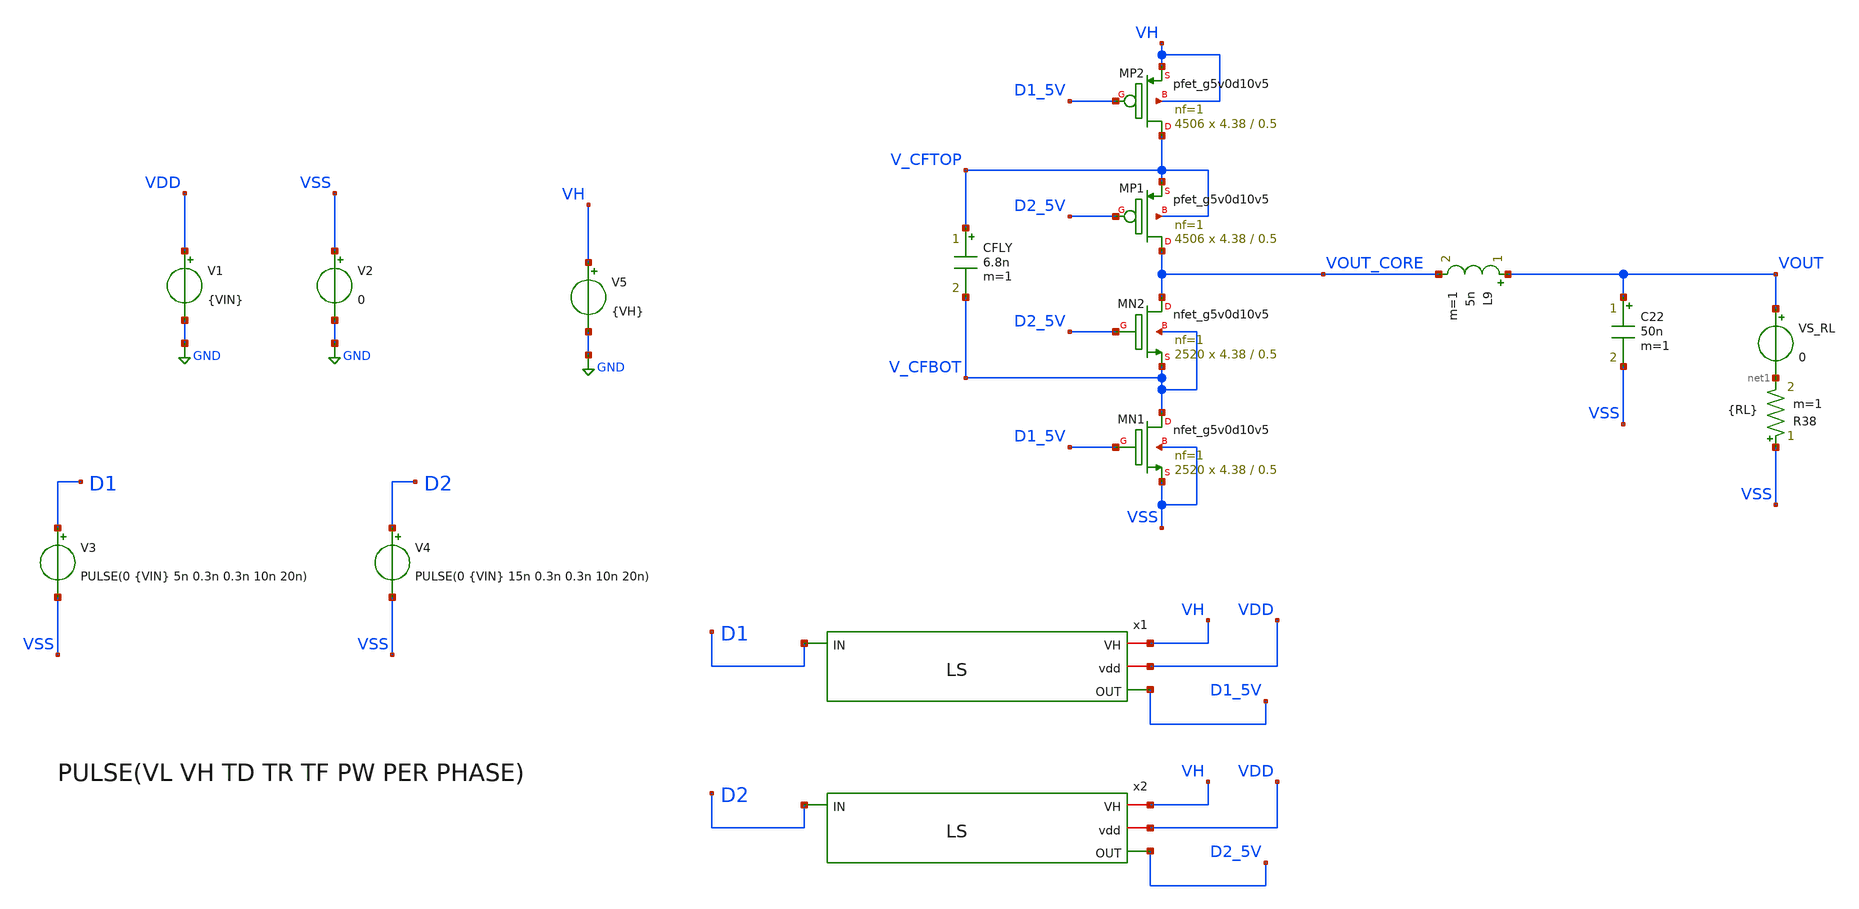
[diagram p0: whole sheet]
** sch_path: xschem/dev_switches/DCDC_v1p3_100MHz_NMOS_PMOS_jm.sch
**.subckt DCDC_v1p3_100MHz_NMOS_PMOS_jm
XMN2 VOUT_CORE D2_5V V_CFBOT V_CFBOT sky130_fd_pr__nfet_g5v0d10v5 L=0.5 W=4.38 nf=1 ad='int((nf+1)/2) * W/nf * 0.29'
+ as='int((nf+2)/2) * W/nf * 0.29' pd='2*int((nf+1)/2) * (W/nf + 0.29)' ps='2*int((nf+2)/2) * (W/nf + 0.29)'
+ nrd='0.29 / W' nrs='0.29 / W' sa=0 sb=0 sd=0 mult=2520 m=2520
XMN1 V_CFBOT D1_5V VSS VSS sky130_fd_pr__nfet_g5v0d10v5 L=0.5 W=4.38 nf=1 ad='int((nf+1)/2) * W/nf * 0.29'
+ as='int((nf+2)/2) * W/nf * 0.29' pd='2*int((nf+1)/2) * (W/nf + 0.29)' ps='2*int((nf+2)/2) * (W/nf + 0.29)'
+ nrd='0.29 / W' nrs='0.29 / W' sa=0 sb=0 sd=0 mult=2520 m=2520
CFLY V_CFTOP V_CFBOT 6.8n m=1
V1 VDD GND {VIN}
V3 D1 VSS PULSE(0 {VIN} 5n 0.3n 0.3n 10n 20n)
V2 VSS GND 0
V4 D2 VSS PULSE(0 {VIN} 15n 0.3n 0.3n 10n 20n)
L9 VOUT VOUT_CORE 5n m=1
C22 VOUT VSS 50n m=1
R38 VSS net1 {RL} m=1
VS_RL VOUT net1 0
V5 VH GND {VH}
XMP2 V_CFTOP D1_5V VH VH sky130_fd_pr__pfet_g5v0d10v5 L=0.5 W=4.38 nf=1 ad='int((nf+1)/2) * W/nf * 0.29'
+ as='int((nf+2)/2) * W/nf * 0.29' pd='2*int((nf+1)/2) * (W/nf + 0.29)' ps='2*int((nf+2)/2) * (W/nf + 0.29)'
+ nrd='0.29 / W' nrs='0.29 / W' sa=0 sb=0 sd=0 mult=4506 m=4506
XMP1 VOUT_CORE D2_5V V_CFTOP V_CFTOP sky130_fd_pr__pfet_g5v0d10v5 L=0.5 W=4.38 nf=1 ad='int((nf+1)/2) * W/nf * 0.29'
+ as='int((nf+2)/2) * W/nf * 0.29' pd='2*int((nf+1)/2) * (W/nf + 0.29)' ps='2*int((nf+2)/2) * (W/nf + 0.29)'
+ nrd='0.29 / W' nrs='0.29 / W' sa=0 sb=0 sd=0 mult=4506 m=4506
x1 VH VDD D1_5V D1 LS
x2 VH VDD D2_5V D2 LS
**** begin user architecture code


.param VIN = 1.8
.param VH = 5
*.param RL = 500
.param RL = 8.3
.option scale=1e-6
*.option temp=70
.ic v(V_CFTOP) = VIN/2
.ic v(V_CFBOT) = 0
*.probe vd(MP2:G:S)

.param mc_mm_switch=0
*.lib /usr/share/pdk/sky130A/libs.tech/ngspice/sky130.lib.spice tt
*.lib /foss/pdk/sky130A/libs.tech/ngspice/sky130.lib.spice TT
.lib /home/jorge/Documents/Postdoc/share/pdk/sky130A/libs.tech/ngspice/sky130.lib.spice tt
*.include /usr/share/pdk/sky130A/libs.ref/sky130_fd_sc_hvl/spice/sky130_fd_sc_hvl.spice
*.include /home/jorge/Documents/Postdoc/share/pdk/sky130A/libs.ref/sky130_fd_sc_hvl/spice/sky130_fd_sc_hvl.spice
.options savecurrents
.control
save all
tran 0.4n 2u
write DCDC_v1p3_100MHz_NMOS_PMOS.raw
.endc


**** end user architecture code
**.ends
.GLOBAL GND
.end
